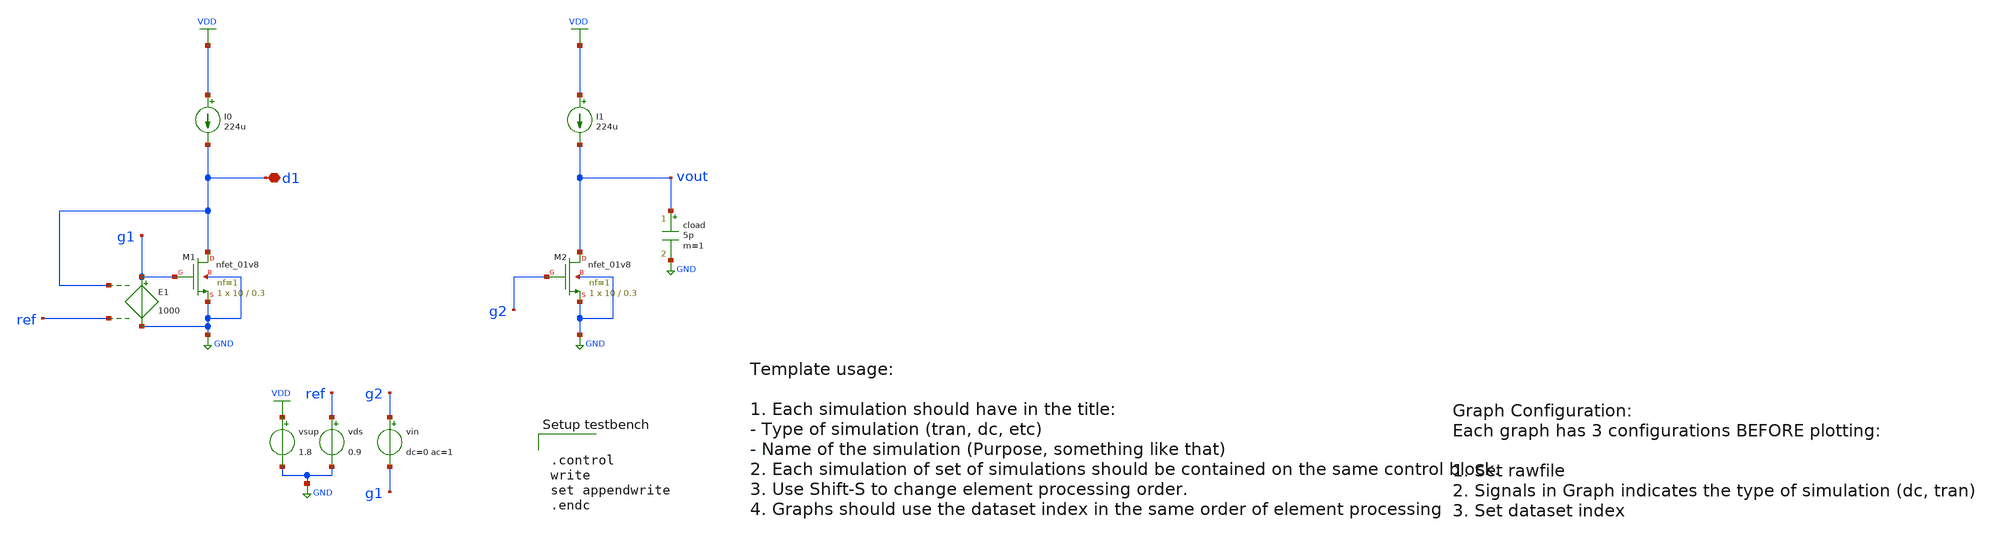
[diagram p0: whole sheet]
** sch_path: samples/sky130/nmos/test/cs_amp_full.sch

*.lib $env(PDK_ROOT)/$env(PDK)/libs.tech/ngspice/sky130.lib.spice tt
.lib $env(PDK_ROOT)/$env(PDK)/libs.tech/ngspice/sky130.lib.spice.tt.red tt


.control
write
set appendwrite
.endc


**.subckt cs_amp_full d1
*.iopin d1
E1 g1 GND d1 ref 1000
I0 VDD d1 224u
I1 VDD vout 224u
XM1 d1 g1 GND GND sky130_fd_pr__nfet_01v8 L=0.3 W=10 nf=1 ad='int((nf+1)/2) * W/nf * 0.29' as='int((nf+2)/2) * W/nf * 0.29'
+ pd='2*int((nf+1)/2) * (W/nf + 0.29)' ps='2*int((nf+2)/2) * (W/nf + 0.29)' nrd='0.29 / W' nrs='0.29 / W'
+ sa=0 sb=0 sd=0 mult=1 m=1
XM2 vout g2 GND GND sky130_fd_pr__nfet_01v8 L=0.3 W=10 nf=1 ad='int((nf+1)/2) * W/nf * 0.29' as='int((nf+2)/2) * W/nf * 0.29'
+ pd='2*int((nf+1)/2) * (W/nf + 0.29)' ps='2*int((nf+2)/2) * (W/nf + 0.29)' nrd='0.29 / W' nrs='0.29 / W'
+ sa=0 sb=0 sd=0 mult=1 m=1
vsup VDD GND 1.8
vds ref GND 0.9
vin g2 g1 dc=0 ac=1
cload vout GND 5p m=1
**** begin user architecture code


.control

ac dec 100 1 1T
* plot vdb(vout)

write

.endc



.control
save all

save @m.xm2.msky130_fd_pr__nfet_01v8[gm]
save @m.xm2.msky130_fd_pr__nfet_01v8[id]
save @m.xm2.msky130_fd_pr__nfet_01v8[gds]

dc vin -0.01 0.01 0.001

let gdsn = @m.xm2.msky130_fd_pr__nfet_01v8[gds]
let gmn = @m.xm2.msky130_fd_pr__nfet_01v8[gm]
let idn = @m.xm2.msky130_fd_pr__nfet_01v8[id]
let ao = gmn / gdsn

*plot deriv(vout) vs vout ao vs vout

write

.endc

**** end user architecture code
**.ends
.GLOBAL GND
.GLOBAL VDD
.end
